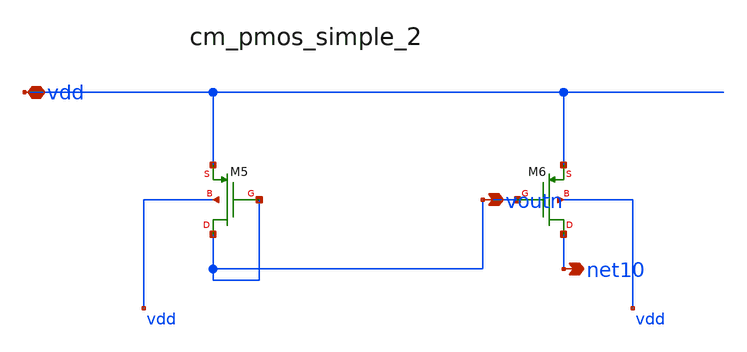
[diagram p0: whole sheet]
** sch_path: analog-db/raw/ldo_001_analoggym_basic/hier/blocks/cm_pmos_simple_2.sch
**.subckt cm_pmos_simple_2 vdd voutn net10
*.iopin vdd
*.opin voutn
*.opin net10
XM5 voutn voutn vdd vdd sg13_lv_pmos w=x_dut_xm5_w l=x_dut_xm5_l ng=1 m=x_dut_xm5_m
XM6 net10 voutn vdd vdd sg13_lv_pmos w=x_dut_xm6_w l=x_dut_xm6_l ng=1 m=x_dut_xm6_m
**.ends
.end
